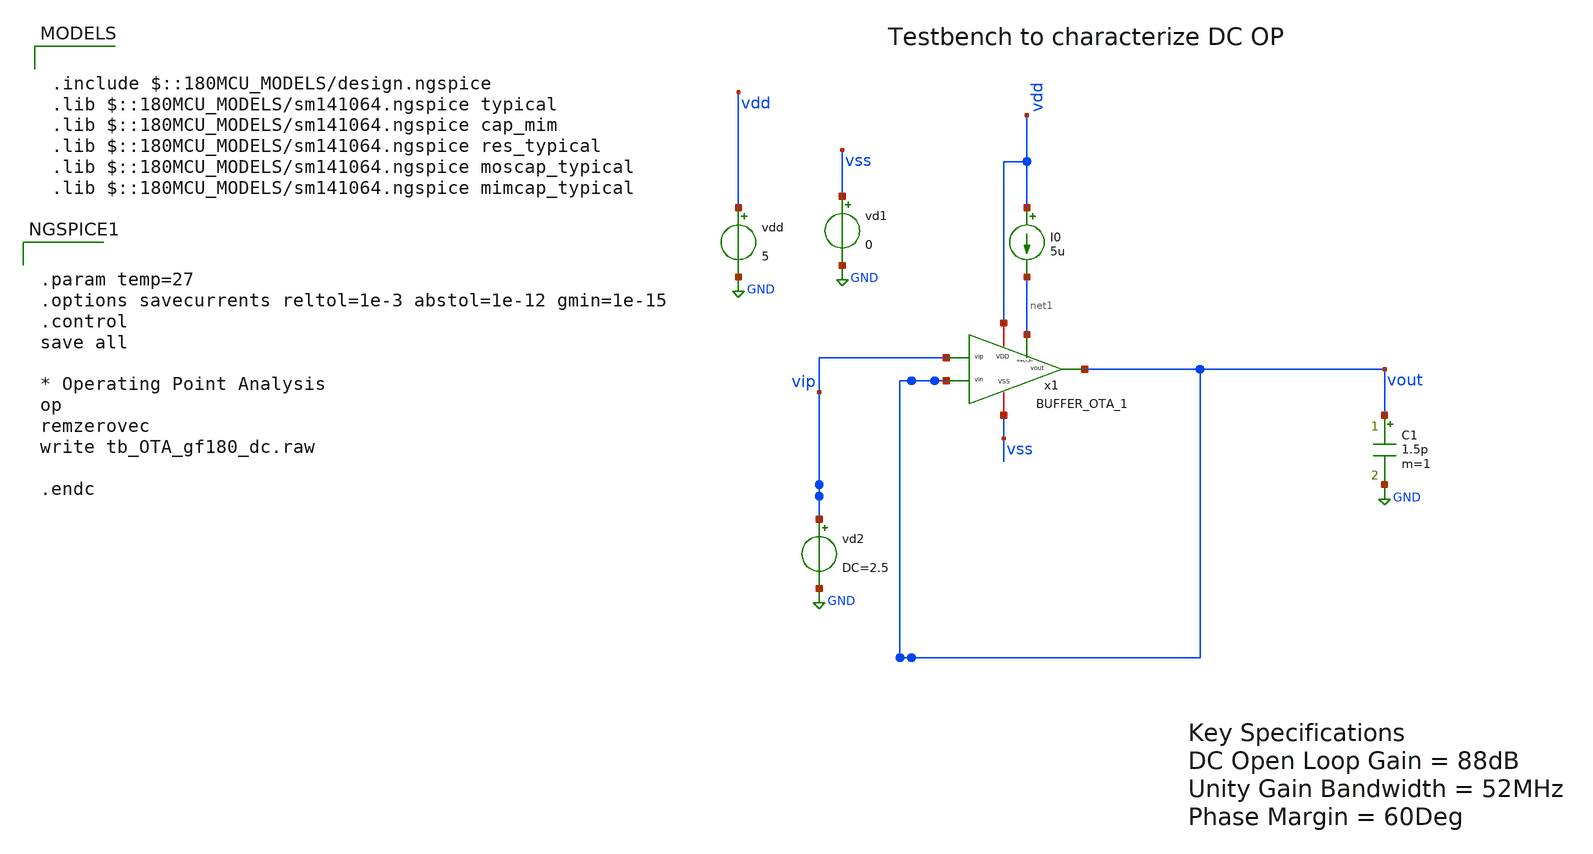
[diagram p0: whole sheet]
** sch_path: xschem/tb_OTA_gf180_dc.sch
**.subckt tb_OTA_gf180_dc
vdd vdd GND 5
vd1 vss GND 0
vd2 vip GND DC=2.5
C1 vout GND 1.5p m=1
I0 vdd net1 5u
x1 vdd vip vout vout net1 vss BUFFER_OTA_1
**** begin user architecture code

.include $::180MCU_MODELS/design.ngspice
.lib $::180MCU_MODELS/sm141064.ngspice typical
.lib $::180MCU_MODELS/sm141064.ngspice cap_mim
.lib $::180MCU_MODELS/sm141064.ngspice res_typical
.lib $::180MCU_MODELS/sm141064.ngspice moscap_typical
.lib $::180MCU_MODELS/sm141064.ngspice mimcap_typical



.param temp=27
.options savecurrents reltol=1e-3 abstol=1e-12 gmin=1e-15
.control
save all

* Operating Point Analysis
op
remzerovec
write tb_OTA_gf180_dc.raw

.endc


**** end user architecture code
**.ends
.GLOBAL GND
.end
